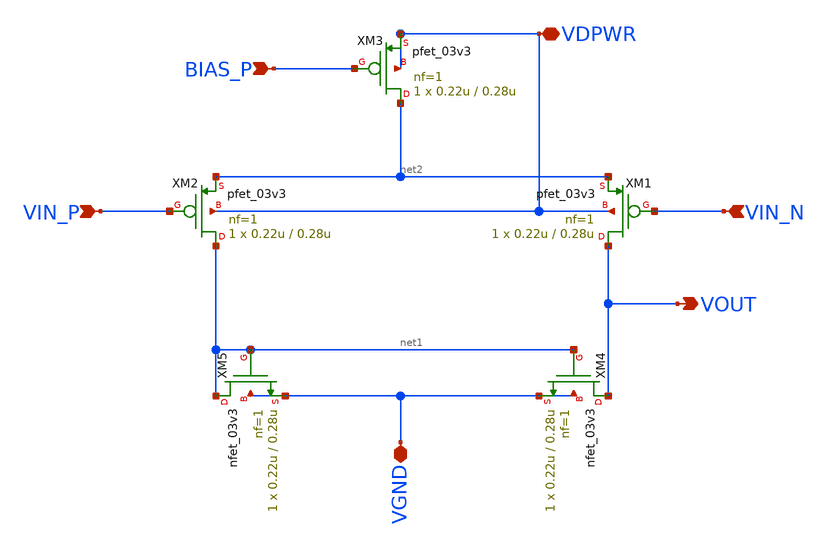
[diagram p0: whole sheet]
** sch_path: xschem/5t_ota.sch
**.subckt 5t_ota VOUT VIN_P VIN_N BIAS_P VDPWR VGND
*.opin VOUT
*.ipin VIN_P
*.ipin VIN_N
*.ipin BIAS_P
*.iopin VDPWR
*.iopin VGND
XM1 VOUT VIN_N net2 VDPWR pfet_03v3 L=0.28u W=0.22u nf=1 ad='int((nf+1)/2) * W/nf * 0.18u' as='int((nf+2)/2) * W/nf * 0.18u'
+ pd='2*int((nf+1)/2) * (W/nf + 0.18u)' ps='2*int((nf+2)/2) * (W/nf + 0.18u)' nrd='0.18u / W' nrs='0.18u / W'
+ sa=0 sb=0 sd=0 m=1
XM2 net1 VIN_P net2 VDPWR pfet_03v3 L=0.28u W=0.22u nf=1 ad='int((nf+1)/2) * W/nf * 0.18u' as='int((nf+2)/2) * W/nf * 0.18u'
+ pd='2*int((nf+1)/2) * (W/nf + 0.18u)' ps='2*int((nf+2)/2) * (W/nf + 0.18u)' nrd='0.18u / W' nrs='0.18u / W'
+ sa=0 sb=0 sd=0 m=1
XM3 net2 BIAS_P VDPWR VDPWR pfet_03v3 L=0.28u W=0.22u nf=1 ad='int((nf+1)/2) * W/nf * 0.18u' as='int((nf+2)/2) * W/nf * 0.18u'
+ pd='2*int((nf+1)/2) * (W/nf + 0.18u)' ps='2*int((nf+2)/2) * (W/nf + 0.18u)' nrd='0.18u / W' nrs='0.18u / W'
+ sa=0 sb=0 sd=0 m=1
XM4 VOUT net1 VGND VGND nfet_03v3 L=0.28u W=0.22u nf=1 ad='int((nf+1)/2) * W/nf * 0.18u' as='int((nf+2)/2) * W/nf * 0.18u'
+ pd='2*int((nf+1)/2) * (W/nf + 0.18u)' ps='2*int((nf+2)/2) * (W/nf + 0.18u)' nrd='0.18u / W' nrs='0.18u / W'
+ sa=0 sb=0 sd=0 m=1
XM5 net1 net1 VGND VGND nfet_03v3 L=0.28u W=0.22u nf=1 ad='int((nf+1)/2) * W/nf * 0.18u' as='int((nf+2)/2) * W/nf * 0.18u'
+ pd='2*int((nf+1)/2) * (W/nf + 0.18u)' ps='2*int((nf+2)/2) * (W/nf + 0.18u)' nrd='0.18u / W' nrs='0.18u / W'
+ sa=0 sb=0 sd=0 m=1
**.ends
.end
